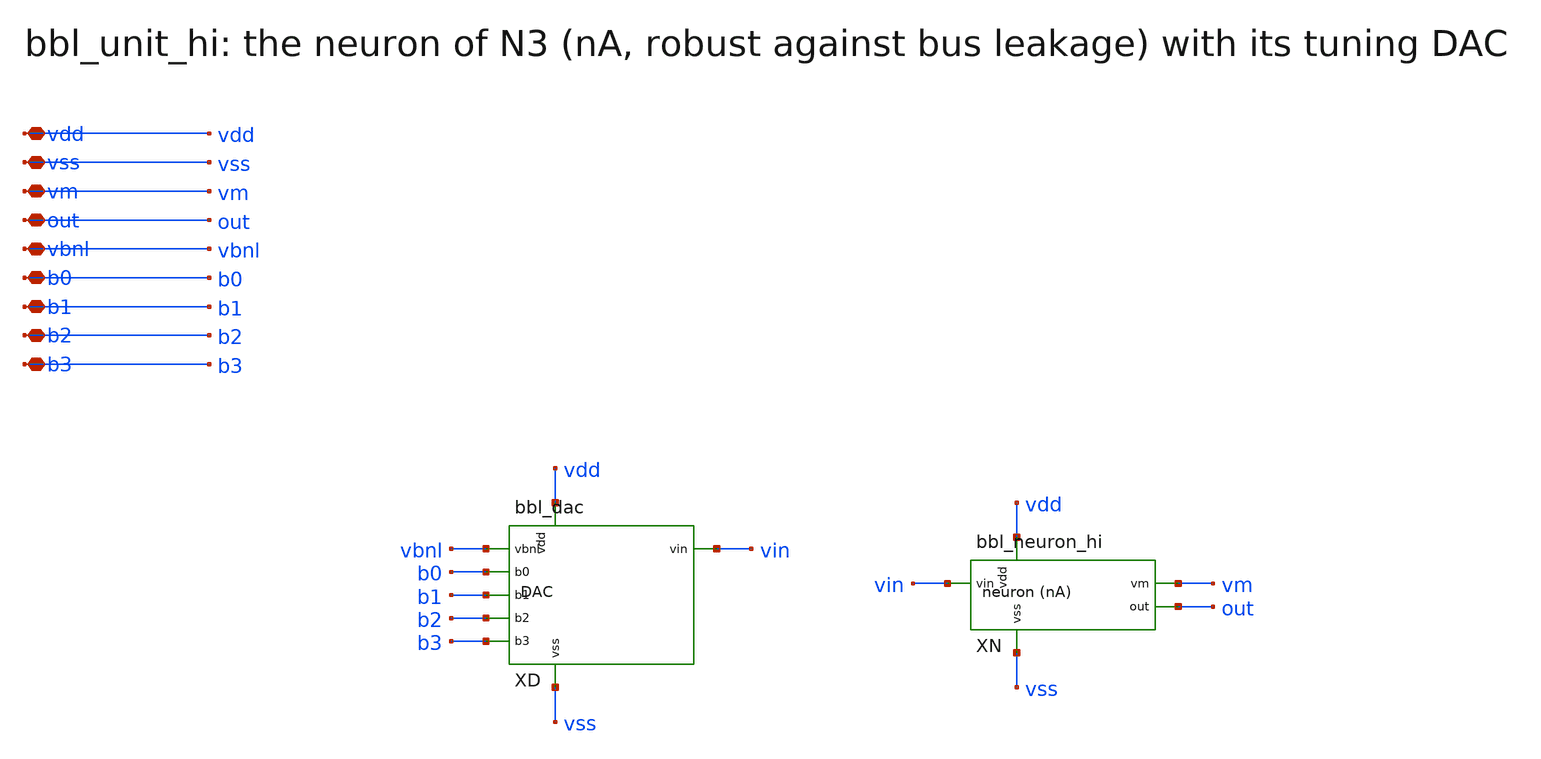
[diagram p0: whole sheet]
** sch_path: schematic/xschem/bbl_unit_hi.sch
**.subckt bbl_unit_hi vdd vss vm out vbnl b0 b1 b2 b3
*.iopin vdd
*.iopin vss
*.iopin vm
*.iopin out
*.iopin vbnl
*.iopin b0
*.iopin b1
*.iopin b2
*.iopin b3
XN vdd vss vm out vin bbl_neuron_hi
XD vdd vss vin vbnl b0 b1 b2 b3 bbl_dac
**.ends

* expanding   symbol:  bbl_neuron_hi.sym # of pins=5
** sym_path: schematic/xschem/bbl_neuron_hi.sym
** sch_path: schematic/xschem/bbl_neuron_hi.sch
.subckt bbl_neuron_hi vdd vss vm out vin
*.iopin vdd
*.iopin vss
*.iopin vm
*.iopin out
*.iopin vin
XMR3 vm vin vdd vdd sg13_hv_pmos w=48u l=3u ng=8 m=1 mm_ok=1
XC1 vdd vm vdd vdd sg13_hv_pmos w=225u l=10u ng=18 m=1 mm_ok=1
XM2 vm rst vss vss sg13_hv_nmos w=40u l=0.45u ng=8 m=1 mm_ok=1
XM3 vm out vdd vdd sg13_hv_pmos w=0.3u l=4u ng=1 m=1 mm_ok=1
XMR1 out vss vdd vdd sg13_hv_pmos w=0.3u l=20u ng=1 m=1 mm_ok=1
XM1 out vm vss vss sg13_hv_nmos w=1u l=1u ng=1 m=1 mm_ok=1
XMR5A slow outb vss vss sg13_hv_nmos w=3u l=0.45u ng=1 m=1 mm_ok=1
XMR5B slow vin vdd vdd sg13_hv_pmos w=10u l=0.45u ng=2 m=1 mm_ok=1
XC2 vss slow vss vss sg13_hv_nmos w=60u l=10u ng=6 m=1 mm_ok=1
XM4 rst slow vdd vdd sg13_hv_pmos w=10u l=0.45u ng=2 m=1 mm_ok=1
XMR2 rst vdd vss vss sg13_hv_nmos w=0.3u l=20u ng=1 m=1 mm_ok=1
XMQ out outb vdd vdd sg13_hv_pmos w=0.3u l=3u ng=1 m=1 mm_ok=1
XMIP outb out vdd vdd sg13_hv_pmos w=3u l=0.45u ng=1 m=1 mm_ok=1
XMIN outb out vss vss sg13_hv_nmos w=0.3u l=4u ng=1 m=1 mm_ok=1
.ends


* expanding   symbol:  bbl_dac.sym # of pins=8
** sym_path: schematic/xschem/bbl_dac.sym
** sch_path: schematic/xschem/bbl_dac.sch
.subckt bbl_dac vdd vss vin vbnl b0 b1 b2 b3
*.iopin vdd
*.iopin vss
*.iopin vin
*.iopin vbnl
*.iopin b0
*.iopin b1
*.iopin b2
*.iopin b3
XMD vin vin vdd vdd sg13_hv_pmos w=3u l=3u ng=1 m=1 mm_ok=1
XMH vin vbnl vss vss sg13_hv_nmos w=0.3u l=9u ng=1 m=1 mm_ok=1
XMU0 vin vbnl s0 vss sg13_hv_nmos w=0.3u l=2u ng=1 m=1 mm_ok=1
XMU1 vin vbnl s1 vss sg13_hv_nmos w=0.6u l=2u ng=2 m=1 mm_ok=1
XMU2 vin vbnl s2 vss sg13_hv_nmos w=1.2u l=2u ng=4 m=1 mm_ok=1
XMU3 vin vbnl s3 vss sg13_hv_nmos w=2.4u l=2u ng=8 m=1 mm_ok=1
XMS0 s0 b0 vss vss sg13_hv_nmos w=0.3u l=0.45u ng=1 m=1 mm_ok=1
XMS1 s1 b1 vss vss sg13_hv_nmos w=0.6u l=0.45u ng=2 m=1 mm_ok=1
XMS2 s2 b2 vss vss sg13_hv_nmos w=1.2u l=0.45u ng=4 m=1 mm_ok=1
XMS3 s3 b3 vss vss sg13_hv_nmos w=2.4u l=0.45u ng=8 m=1 mm_ok=1
.ends

.end
